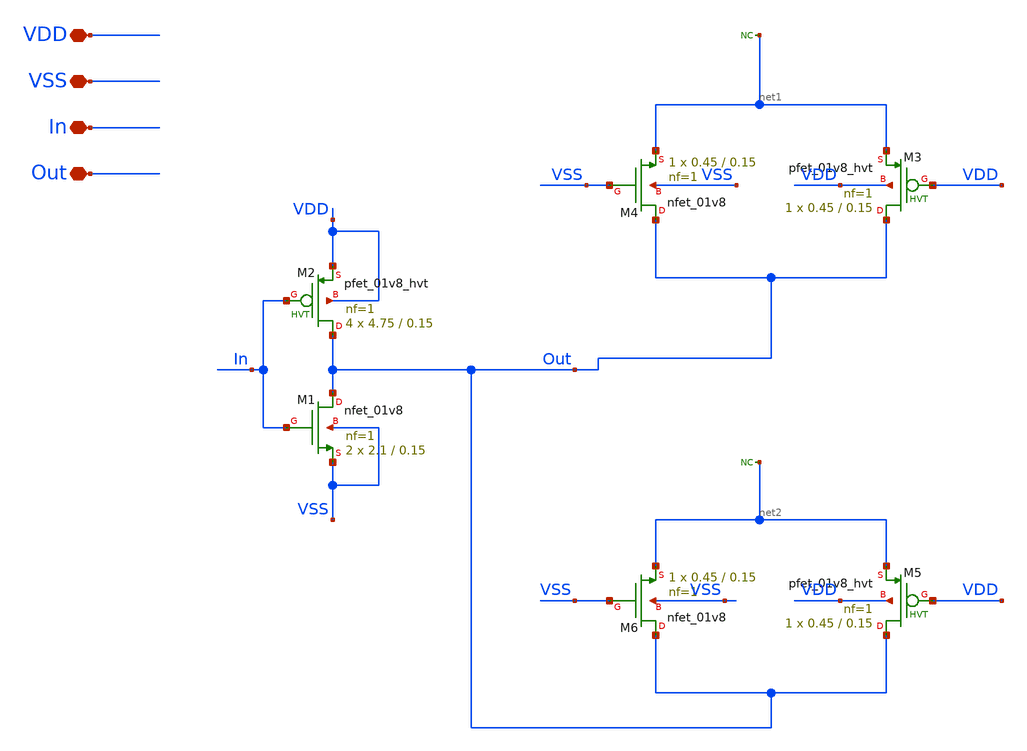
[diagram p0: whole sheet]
** sch_path: HVT/RingStage/RingStage.sch
**.subckt RingStage In Out VDD VSS
*.iopin In
*.iopin Out
*.iopin VDD
*.iopin VSS
XM2 Out In VDD VDD sky130_fd_pr__pfet_01v8_hvt L=0.15 W=4.75 nf=1 ad='int((nf+1)/2) * W/nf * 0.29' as='int((nf+2)/2) * W/nf * 0.29'
+ pd='2*int((nf+1)/2) * (W/nf + 0.29)' ps='2*int((nf+2)/2) * (W/nf + 0.29)' nrd='0.29 / W' nrs='0.29 / W'
+ sa=0 sb=0 sd=0 mult=4 m=4
XM1 Out In VSS VSS sky130_fd_pr__nfet_01v8 L=0.15 W=2.1 nf=1 ad='int((nf+1)/2) * W/nf * 0.29' as='int((nf+2)/2) * W/nf * 0.29'
+ pd='2*int((nf+1)/2) * (W/nf + 0.29)' ps='2*int((nf+2)/2) * (W/nf + 0.29)' nrd='0.29 / W' nrs='0.29 / W'
+ sa=0 sb=0 sd=0 mult=2 m=2
XM3 Out VDD net1 VDD sky130_fd_pr__pfet_01v8_hvt L=0.15 W=0.45 nf=1 ad='int((nf+1)/2) * W/nf * 0.29'
+ as='int((nf+2)/2) * W/nf * 0.29' pd='2*int((nf+1)/2) * (W/nf + 0.29)' ps='2*int((nf+2)/2) * (W/nf + 0.29)'
+ nrd='0.29 / W' nrs='0.29 / W' sa=0 sb=0 sd=0 mult=1 m=1
XM4 Out VSS net1 VSS sky130_fd_pr__nfet_01v8 L=0.15 W=0.45 nf=1 ad='int((nf+1)/2) * W/nf * 0.29' as='int((nf+2)/2) * W/nf * 0.29'
+ pd='2*int((nf+1)/2) * (W/nf + 0.29)' ps='2*int((nf+2)/2) * (W/nf + 0.29)' nrd='0.29 / W' nrs='0.29 / W'
+ sa=0 sb=0 sd=0 mult=1 m=1
XM5 Out VDD net2 VDD sky130_fd_pr__pfet_01v8_hvt L=0.15 W=0.45 nf=1 ad='int((nf+1)/2) * W/nf * 0.29'
+ as='int((nf+2)/2) * W/nf * 0.29' pd='2*int((nf+1)/2) * (W/nf + 0.29)' ps='2*int((nf+2)/2) * (W/nf + 0.29)'
+ nrd='0.29 / W' nrs='0.29 / W' sa=0 sb=0 sd=0 mult=1 m=1
XM6 Out VSS net2 VSS sky130_fd_pr__nfet_01v8 L=0.15 W=0.45 nf=1 ad='int((nf+1)/2) * W/nf * 0.29' as='int((nf+2)/2) * W/nf * 0.29'
+ pd='2*int((nf+1)/2) * (W/nf + 0.29)' ps='2*int((nf+2)/2) * (W/nf + 0.29)' nrd='0.29 / W' nrs='0.29 / W'
+ sa=0 sb=0 sd=0 mult=1 m=1
* noconn #net1
* noconn #net2
**.ends
.end
